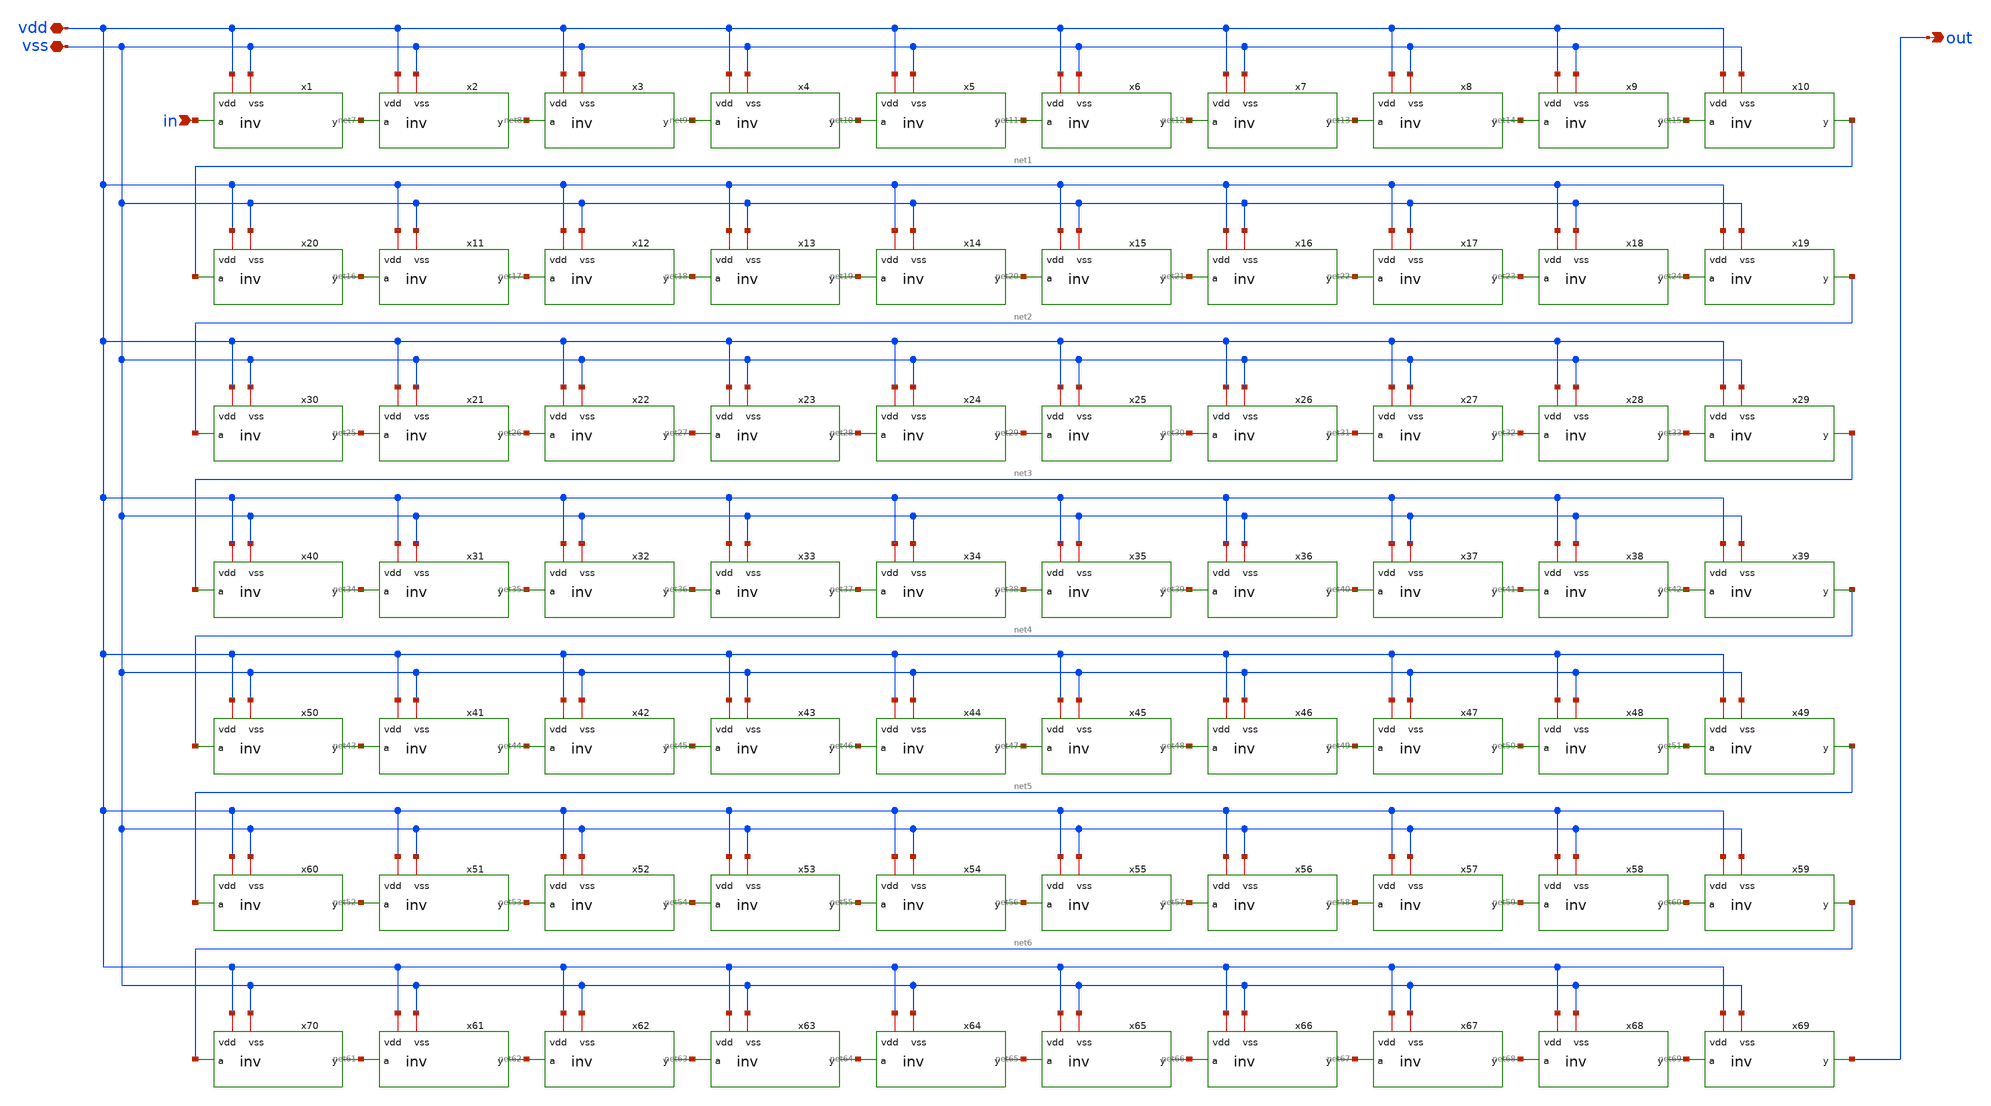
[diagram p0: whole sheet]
** sch_path: member_project/ice458/dynamic_comparator/xschem/delay.sch
**.subckt delay in out vdd vss
*.ipin in
*.opin out
*.iopin vdd
*.iopin vss
x1 vdd in net7 vss inv
x2 vdd net7 net8 vss inv
x3 vdd net8 net9 vss inv
x4 vdd net9 net10 vss inv
x5 vdd net10 net11 vss inv
x6 vdd net11 net12 vss inv
x7 vdd net12 net13 vss inv
x8 vdd net13 net14 vss inv
x9 vdd net14 net15 vss inv
x10 vdd net15 net1 vss inv
x11 vdd net16 net17 vss inv
x12 vdd net17 net18 vss inv
x13 vdd net18 net19 vss inv
x14 vdd net19 net20 vss inv
x15 vdd net20 net21 vss inv
x16 vdd net21 net22 vss inv
x17 vdd net22 net23 vss inv
x18 vdd net23 net24 vss inv
x19 vdd net24 net2 vss inv
x20 vdd net1 net16 vss inv
x21 vdd net25 net26 vss inv
x22 vdd net26 net27 vss inv
x23 vdd net27 net28 vss inv
x24 vdd net28 net29 vss inv
x25 vdd net29 net30 vss inv
x26 vdd net30 net31 vss inv
x27 vdd net31 net32 vss inv
x28 vdd net32 net33 vss inv
x29 vdd net33 net3 vss inv
x30 vdd net2 net25 vss inv
x31 vdd net34 net35 vss inv
x32 vdd net35 net36 vss inv
x33 vdd net36 net37 vss inv
x34 vdd net37 net38 vss inv
x35 vdd net38 net39 vss inv
x36 vdd net39 net40 vss inv
x37 vdd net40 net41 vss inv
x38 vdd net41 net42 vss inv
x39 vdd net42 net4 vss inv
x40 vdd net3 net34 vss inv
x41 vdd net43 net44 vss inv
x42 vdd net44 net45 vss inv
x43 vdd net45 net46 vss inv
x44 vdd net46 net47 vss inv
x45 vdd net47 net48 vss inv
x46 vdd net48 net49 vss inv
x47 vdd net49 net50 vss inv
x48 vdd net50 net51 vss inv
x49 vdd net51 net5 vss inv
x50 vdd net4 net43 vss inv
x51 vdd net52 net53 vss inv
x52 vdd net53 net54 vss inv
x53 vdd net54 net55 vss inv
x54 vdd net55 net56 vss inv
x55 vdd net56 net57 vss inv
x56 vdd net57 net58 vss inv
x57 vdd net58 net59 vss inv
x58 vdd net59 net60 vss inv
x59 vdd net60 net6 vss inv
x60 vdd net5 net52 vss inv
x61 vdd net61 net62 vss inv
x62 vdd net62 net63 vss inv
x63 vdd net63 net64 vss inv
x64 vdd net64 net65 vss inv
x65 vdd net65 net66 vss inv
x66 vdd net66 net67 vss inv
x67 vdd net67 net68 vss inv
x68 vdd net68 net69 vss inv
x69 vdd net69 out vss inv
x70 vdd net6 net61 vss inv
**.ends

* expanding   symbol:  inv.sym # of pins=4
** sym_path: member_project/ice458/dynamic_comparator/xschem/inv.sym
** sch_path: member_project/ice458/dynamic_comparator/xschem/inv.sch
.subckt inv vdd a y vss
*.iopin vdd
*.iopin vss
*.ipin a
*.opin y
XM1 y a vss vss nfet_03v3 L=0.28u W=0.42u nf=1 ad='int((nf+1)/2) * W/nf * 0.18u' as='int((nf+2)/2) * W/nf * 0.18u'
+ pd='2*int((nf+1)/2) * (W/nf + 0.18u)' ps='2*int((nf+2)/2) * (W/nf + 0.18u)' nrd='0.18u / W' nrs='0.18u / W'
+ sa=0 sb=0 sd=0 m=1
XM2 y a vdd vdd pfet_03v3 L=0.28u W=1u nf=1 ad='int((nf+1)/2) * W/nf * 0.18u' as='int((nf+2)/2) * W/nf * 0.18u'
+ pd='2*int((nf+1)/2) * (W/nf + 0.18u)' ps='2*int((nf+2)/2) * (W/nf + 0.18u)' nrd='0.18u / W' nrs='0.18u / W'
+ sa=0 sb=0 sd=0 m=1
.ends

.end
